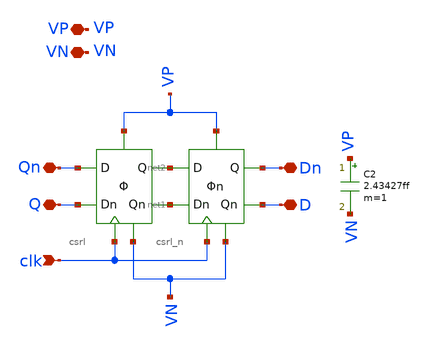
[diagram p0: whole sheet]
** sch_path: csrl/csrl_edge_backup.sch
**.subckt csrl_edge_backup clk D Dn Q Qn VP VN
*.ipin clk
*.iopin D
*.iopin Dn
*.iopin Q
*.iopin Qn
*.iopin VP
*.iopin VN
X1 Qn Q net1 net2 VN clk VP csrl
X2 net2 net1 D Dn VN clk VP csrl_n
C2 VP VN 2.43427ff m=1
**.ends
.end
